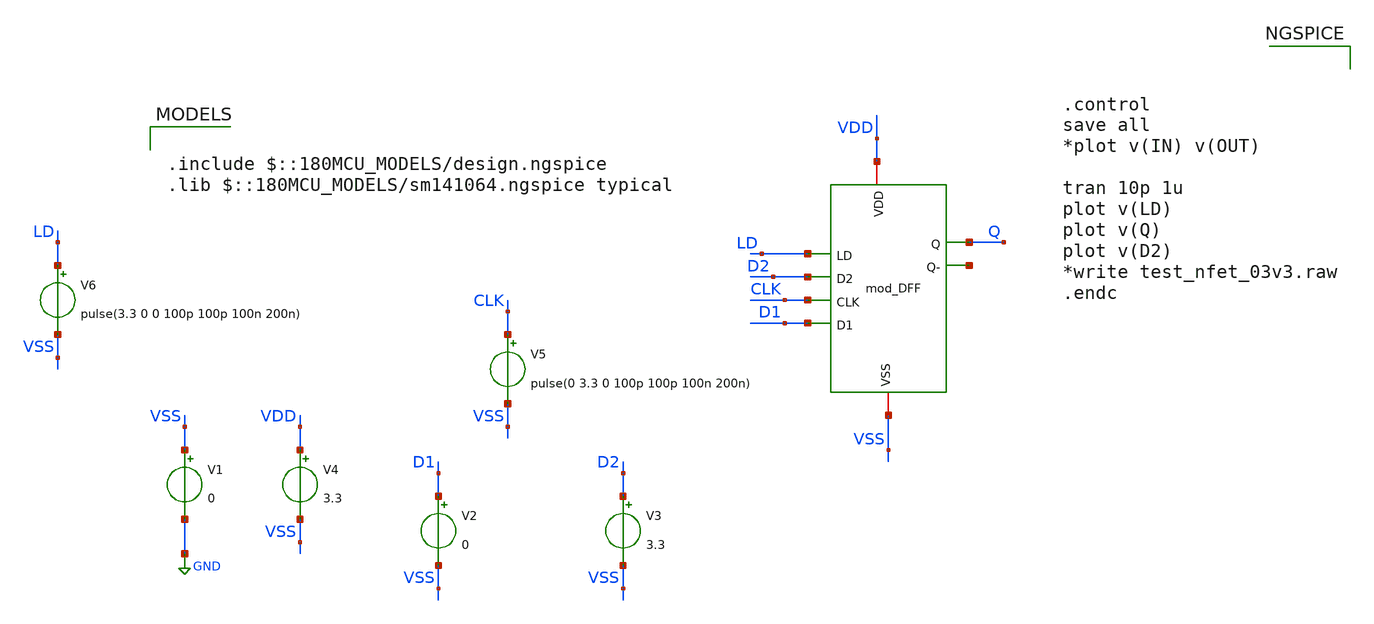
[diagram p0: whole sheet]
** sch_path: Clock_Generator_PAKISTAN_06/Schematics/mod-DFF-tb.sch
**.subckt mod-DFF-tb
x1 VDD LD D2 VSS CLK Q D1 net1 mod_DFF
V4 VDD VSS 3.3
V5 CLK VSS pulse(0 3.3 0 100p 100p 100n 200n)
V1 VSS GND 0
V2 D1 VSS 0
V3 D2 VSS 3.3
V6 LD VSS pulse(3.3 0 0 100p 100p 100n 200n)
**** begin user architecture code

.include $::180MCU_MODELS/design.ngspice
.lib $::180MCU_MODELS/sm141064.ngspice typical




.control
save all
*plot v(IN) v(OUT)

tran 10p 1u
plot v(LD)
plot v(Q)
plot v(D2)
*write test_nfet_03v3.raw
.endc


**** end user architecture code
**.ends
.GLOBAL GND
.end
